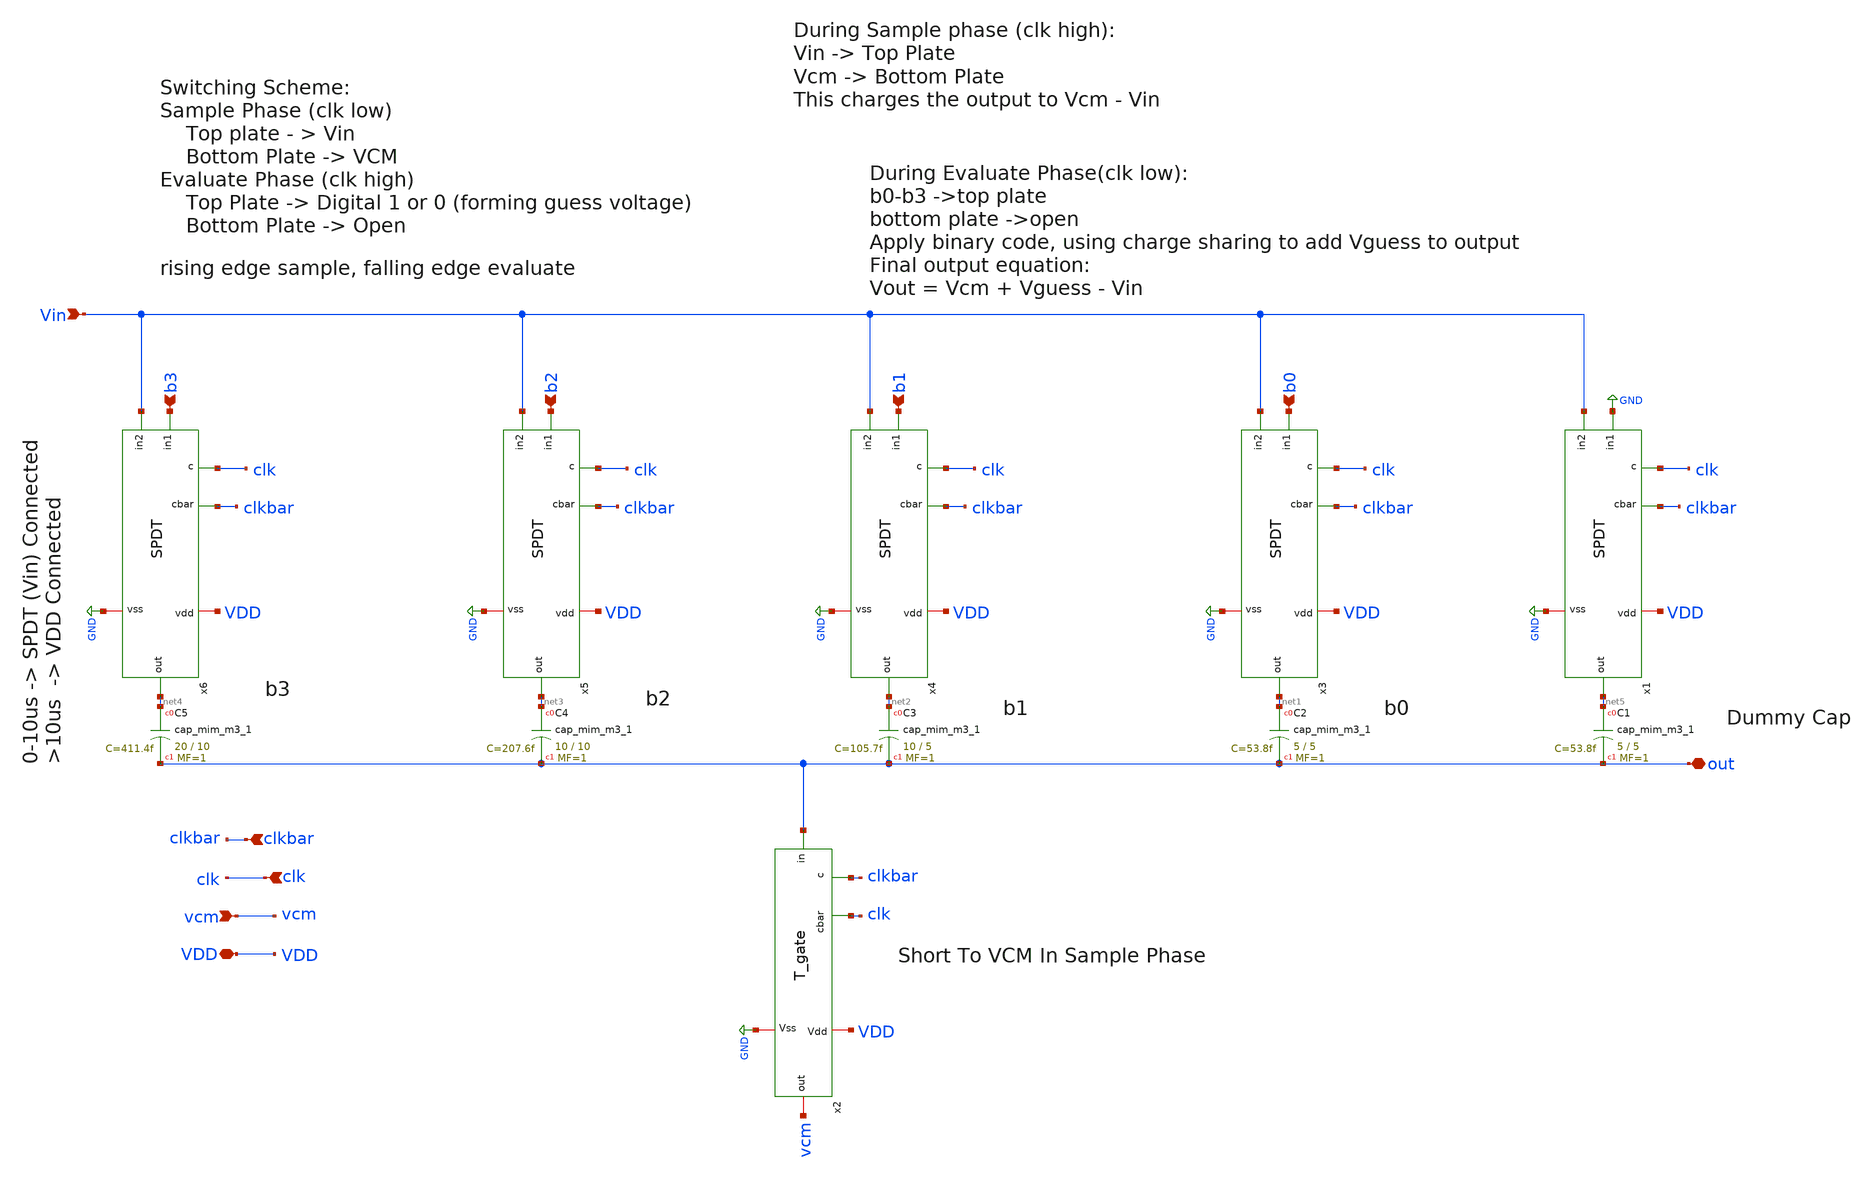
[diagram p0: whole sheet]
** sch_path: ADC/16bit_C2C/MagicAndSpice/CDAC_4bit_VCM_simplified.sch
**.subckt CDAC_4bit_VCM_simplified Vin clk clkbar vcm VDD b3 b2 b1 out b0
*.ipin Vin
*.ipin clk
*.ipin clkbar
*.ipin vcm
*.iopin VDD
*.ipin b3
*.ipin b2
*.ipin b1
*.iopin out
*.ipin b0
XC1 net5 out sky130_fd_pr__cap_mim_m3_1 W=5 L=5 MF=1 m=1
XC2 net1 out sky130_fd_pr__cap_mim_m3_1 W=5 L=5 MF=1 m=1
x2 clkbar vcm out VDD clk GND T_gate
x3 clkbar VDD GND clk b0 net1 Vin SPDT
XC3 net2 out sky130_fd_pr__cap_mim_m3_1 W=10 L=5 MF=1 m=1
x4 clkbar VDD GND clk b1 net2 Vin SPDT
XC4 net3 out sky130_fd_pr__cap_mim_m3_1 W=10 L=10 MF=1 m=1
x5 clkbar VDD GND clk b2 net3 Vin SPDT
XC5 net4 out sky130_fd_pr__cap_mim_m3_1 W=20 L=10 MF=1 m=1
x6 clkbar VDD GND clk b3 net4 Vin SPDT
x1 clkbar VDD GND clk GND net5 Vin SPDT
**.ends
.GLOBAL GND
.end
